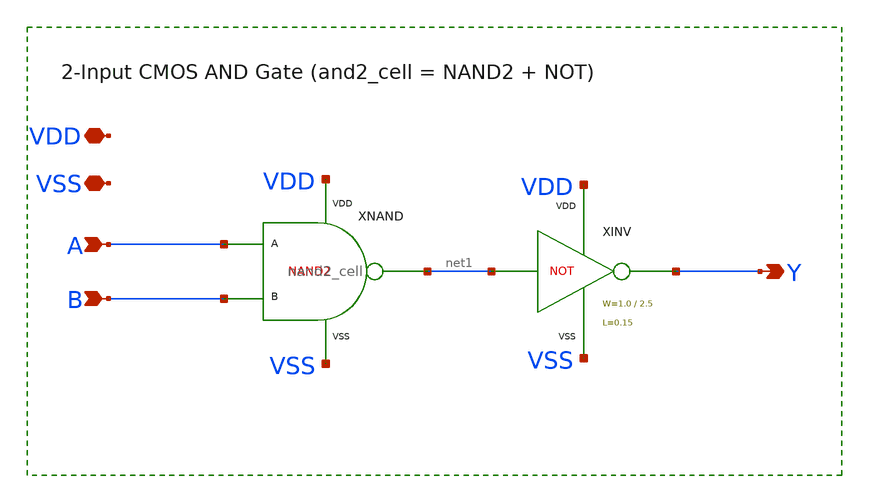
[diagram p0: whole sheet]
** sch_path: sky130-sc-lpf/xschem/and2_cell.sch
**.subckt and2_cell VDD VSS A B Y
*.iopin VDD
*.iopin VSS
*.ipin A
*.ipin B
*.opin Y
XNAND A B net1 VDD VSS nand2_cell
XINV net1 Y VDD VSS inv_cell WN=1.0 WP=2.5 LCH=0.15
**.ends

* expanding   symbol:  nand2_cell.sym # of pins=5
** sym_path: sky130-sc-lpf/xschem/nand2_cell.sym
** sch_path: sky130-sc-lpf/xschem/nand2_cell.sch
.subckt nand2_cell A B Y VDD VSS
*.iopin VDD
*.opin Y
*.iopin VSS
*.ipin A
*.ipin B
XMPA Y A VDD VDD sky130_fd_pr__pfet_01v8 L=0.15 W=2.0 nf=1 ad='int((nf+1)/2) * W/nf * 0.29' as='int((nf+2)/2) * W/nf * 0.29'
+ pd='2*int((nf+1)/2) * (W/nf + 0.29)' ps='2*int((nf+2)/2) * (W/nf + 0.29)' nrd='0.29 / W' nrs='0.29 / W'
+ sa=0 sb=0 sd=0 mult=1 m=1
XMPB Y B VDD VDD sky130_fd_pr__pfet_01v8 L=0.15 W=2.0 nf=1 ad='int((nf+1)/2) * W/nf * 0.29' as='int((nf+2)/2) * W/nf * 0.29'
+ pd='2*int((nf+1)/2) * (W/nf + 0.29)' ps='2*int((nf+2)/2) * (W/nf + 0.29)' nrd='0.29 / W' nrs='0.29 / W'
+ sa=0 sb=0 sd=0 mult=1 m=1
XMNA Y A net1 VSS sky130_fd_pr__nfet_01v8 L=0.15 W=1.6 nf=1 ad='int((1 + 1)/2) * 1.6 / 1 * 0.29' as='int((1 + 2)/2) * 1.6 / 1 * 0.29'
+ pd='2*int((1 + 1)/2) * (1.6 / 1 + 0.29)' ps='2*int((1 + 2)/2) * (1.6 / 1 + 0.29)' nrd='0.29 / 1.6 ' nrs='0.29 / 1.6 '
+ sa=0 sb=0 sd=0 mult=1 m=1
XMNB net1 B VSS VSS sky130_fd_pr__nfet_01v8 L=0.15 W=1.6 nf=1 ad='int((1 + 1)/2) * 1.6 / 1 * 0.29' as='int((1 + 2)/2) * 1.6 / 1 * 0.29'
+ pd='2*int((1 + 1)/2) * (1.6 / 1 + 0.29)' ps='2*int((1 + 2)/2) * (1.6 / 1 + 0.29)' nrd='0.29 / 1.6 ' nrs='0.29 / 1.6 '
+ sa=0 sb=0 sd=0 mult=1 m=1
.ends


* expanding   symbol:  inv_cell.sym # of pins=4
** sym_path: sky130-sc-lpf/xschem/inv_cell.sym
** sch_path: sky130-sc-lpf/xschem/inv_cell.sch
.subckt inv_cell A Y VDD VSS  WN=1.0 WP=2.5 LCH=0.15
*.ipin A
*.opin Y
*.iopin VDD
*.iopin VSS
XMP Y A VDD VDD sky130_fd_pr__pfet_01v8 L='LCH' W='WP' nf=1 ad='WP*0.29' as='WP*0.29' pd='2*(WP+0.29)'
+ ps='2*(WP+0.29)' nrd='0.29/WP' nrs='0.29/WP' sa=0 sb=0 sd=0 mult=1 m=1
XMN Y A VSS VSS sky130_fd_pr__nfet_01v8 L='LCH' W='WN' nf=1 ad='WN*0.29' as='WN*0.29' pd='2*(WN+0.29)'
+ ps='2*(WN+0.29)' nrd='0.29/WN' nrs='0.29/WN' sa=0 sb=0 sd=0 mult=1 m=1
.ends

.end
